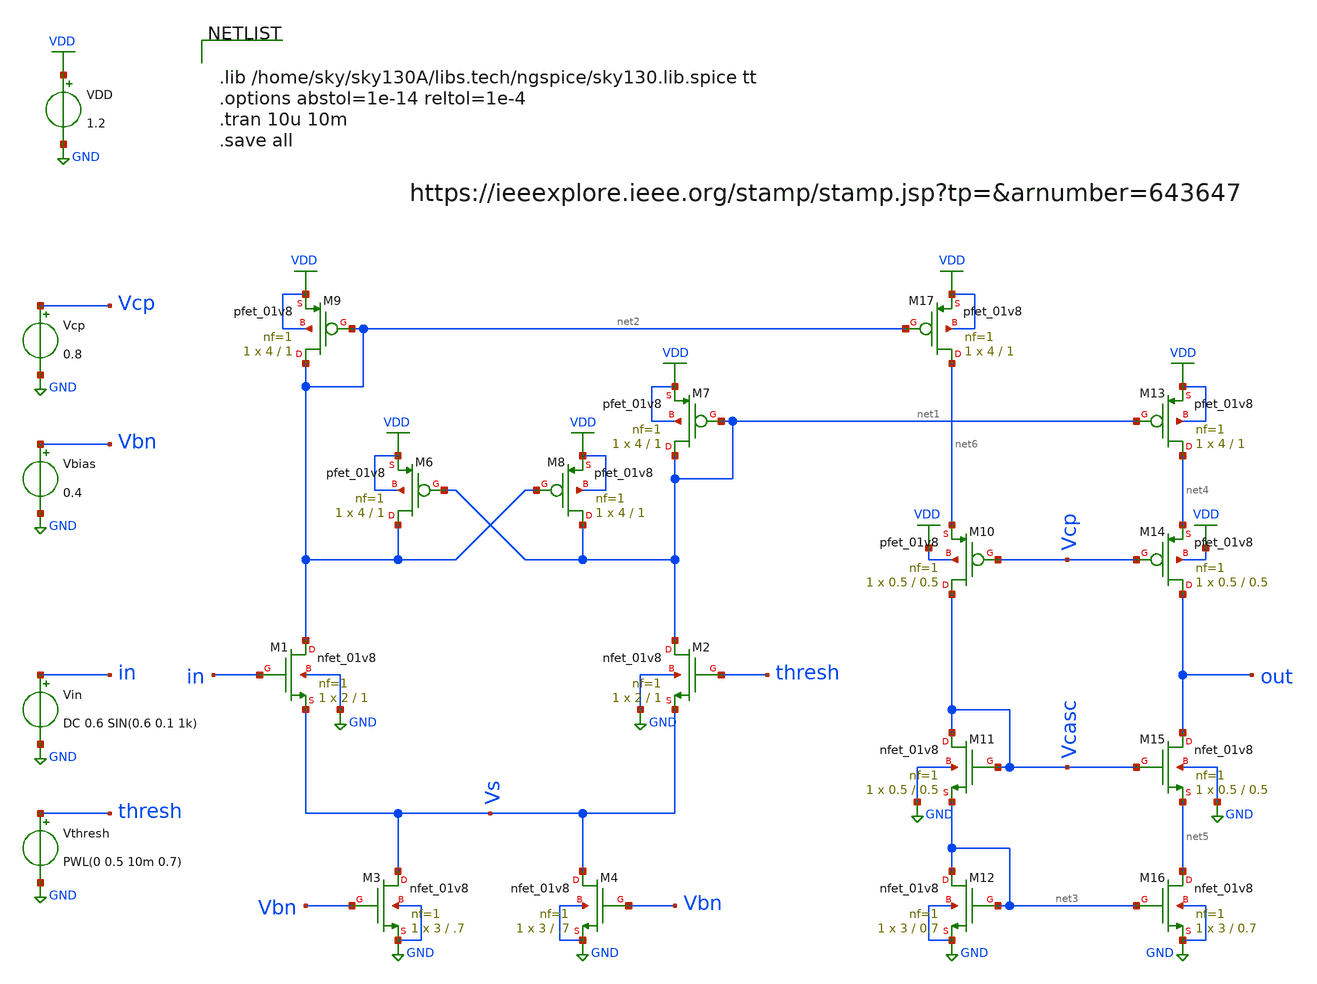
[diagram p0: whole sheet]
** sch_path: xschem/zcd/comparator_tb.sch
**.subckt comparator_tb
XM1 net2 in Vs GND sky130_fd_pr__nfet_01v8 L=1 W=2 nf=1 ad='int((nf+1)/2) * W/nf * 0.29' as='int((nf+2)/2) * W/nf * 0.29'
+ pd='2*int((nf+1)/2) * (W/nf + 0.29)' ps='2*int((nf+2)/2) * (W/nf + 0.29)' nrd='0.29 / W' nrs='0.29 / W'
+ sa=0 sb=0 sd=0 mult=1 m=1
VDD VDD GND 1.2
XM2 net1 thresh Vs GND sky130_fd_pr__nfet_01v8 L=1 W=2 nf=1 ad='int((nf+1)/2) * W/nf * 0.29' as='int((nf+2)/2) * W/nf * 0.29'
+ pd='2*int((nf+1)/2) * (W/nf + 0.29)' ps='2*int((nf+2)/2) * (W/nf + 0.29)' nrd='0.29 / W' nrs='0.29 / W'
+ sa=0 sb=0 sd=0 mult=1 m=1
XM3 Vs Vbn GND GND sky130_fd_pr__nfet_01v8 L=.7 W=3 nf=1 ad='int((nf+1)/2) * W/nf * 0.29' as='int((nf+2)/2) * W/nf * 0.29'
+ pd='2*int((nf+1)/2) * (W/nf + 0.29)' ps='2*int((nf+2)/2) * (W/nf + 0.29)' nrd='0.29 / W' nrs='0.29 / W'
+ sa=0 sb=0 sd=0 mult=1 m=1
XM4 Vs Vbn GND GND sky130_fd_pr__nfet_01v8 L=.7 W=3 nf=1 ad='int((nf+1)/2) * W/nf * 0.29' as='int((nf+2)/2) * W/nf * 0.29'
+ pd='2*int((nf+1)/2) * (W/nf + 0.29)' ps='2*int((nf+2)/2) * (W/nf + 0.29)' nrd='0.29 / W' nrs='0.29 / W'
+ sa=0 sb=0 sd=0 mult=1 m=1
XM6 net2 net1 VDD VDD sky130_fd_pr__pfet_01v8 L=1 W=4 nf=1 ad='int((nf+1)/2) * W/nf * 0.29' as='int((nf+2)/2) * W/nf * 0.29'
+ pd='2*int((nf+1)/2) * (W/nf + 0.29)' ps='2*int((nf+2)/2) * (W/nf + 0.29)' nrd='0.29 / W' nrs='0.29 / W'
+ sa=0 sb=0 sd=0 mult=1 m=1
XM7 net1 net1 VDD VDD sky130_fd_pr__pfet_01v8 L=1 W=4 nf=1 ad='int((nf+1)/2) * W/nf * 0.29' as='int((nf+2)/2) * W/nf * 0.29'
+ pd='2*int((nf+1)/2) * (W/nf + 0.29)' ps='2*int((nf+2)/2) * (W/nf + 0.29)' nrd='0.29 / W' nrs='0.29 / W'
+ sa=0 sb=0 sd=0 mult=1 m=1
XM8 net1 net2 VDD VDD sky130_fd_pr__pfet_01v8 L=1 W=4 nf=1 ad='int((nf+1)/2) * W/nf * 0.29' as='int((nf+2)/2) * W/nf * 0.29'
+ pd='2*int((nf+1)/2) * (W/nf + 0.29)' ps='2*int((nf+2)/2) * (W/nf + 0.29)' nrd='0.29 / W' nrs='0.29 / W'
+ sa=0 sb=0 sd=0 mult=1 m=1
XM9 net2 net2 VDD VDD sky130_fd_pr__pfet_01v8 L=1 W=4 nf=1 ad='int((nf+1)/2) * W/nf * 0.29' as='int((nf+2)/2) * W/nf * 0.29'
+ pd='2*int((nf+1)/2) * (W/nf + 0.29)' ps='2*int((nf+2)/2) * (W/nf + 0.29)' nrd='0.29 / W' nrs='0.29 / W'
+ sa=0 sb=0 sd=0 mult=1 m=1
XM10 Vcasc Vcp net6 VDD sky130_fd_pr__pfet_01v8 L=0.5 W=0.5 nf=1 ad='int((nf+1)/2) * W/nf * 0.29' as='int((nf+2)/2) * W/nf * 0.29'
+ pd='2*int((nf+1)/2) * (W/nf + 0.29)' ps='2*int((nf+2)/2) * (W/nf + 0.29)' nrd='0.29 / W' nrs='0.29 / W'
+ sa=0 sb=0 sd=0 mult=1 m=1
XM11 Vcasc Vcasc net3 GND sky130_fd_pr__nfet_01v8 L=0.5 W=0.5 nf=1 ad='int((nf+1)/2) * W/nf * 0.29' as='int((nf+2)/2) * W/nf * 0.29'
+ pd='2*int((nf+1)/2) * (W/nf + 0.29)' ps='2*int((nf+2)/2) * (W/nf + 0.29)' nrd='0.29 / W' nrs='0.29 / W'
+ sa=0 sb=0 sd=0 mult=1 m=1
XM12 net3 net3 GND GND sky130_fd_pr__nfet_01v8 L=0.7 W=3 nf=1 ad='int((nf+1)/2) * W/nf * 0.29' as='int((nf+2)/2) * W/nf * 0.29'
+ pd='2*int((nf+1)/2) * (W/nf + 0.29)' ps='2*int((nf+2)/2) * (W/nf + 0.29)' nrd='0.29 / W' nrs='0.29 / W'
+ sa=0 sb=0 sd=0 mult=1 m=1
XM13 net4 net1 VDD VDD sky130_fd_pr__pfet_01v8 L=1 W=4 nf=1 ad='int((nf+1)/2) * W/nf * 0.29' as='int((nf+2)/2) * W/nf * 0.29'
+ pd='2*int((nf+1)/2) * (W/nf + 0.29)' ps='2*int((nf+2)/2) * (W/nf + 0.29)' nrd='0.29 / W' nrs='0.29 / W'
+ sa=0 sb=0 sd=0 mult=1 m=1
XM14 out Vcp net4 VDD sky130_fd_pr__pfet_01v8 L=0.5 W=0.5 nf=1 ad='int((nf+1)/2) * W/nf * 0.29' as='int((nf+2)/2) * W/nf * 0.29'
+ pd='2*int((nf+1)/2) * (W/nf + 0.29)' ps='2*int((nf+2)/2) * (W/nf + 0.29)' nrd='0.29 / W' nrs='0.29 / W'
+ sa=0 sb=0 sd=0 mult=1 m=1
XM15 out Vcasc net5 GND sky130_fd_pr__nfet_01v8 L=0.5 W=0.5 nf=1 ad='int((nf+1)/2) * W/nf * 0.29' as='int((nf+2)/2) * W/nf * 0.29'
+ pd='2*int((nf+1)/2) * (W/nf + 0.29)' ps='2*int((nf+2)/2) * (W/nf + 0.29)' nrd='0.29 / W' nrs='0.29 / W'
+ sa=0 sb=0 sd=0 mult=1 m=1
XM16 net5 net3 GND GND sky130_fd_pr__nfet_01v8 L=0.7 W=3 nf=1 ad='int((nf+1)/2) * W/nf * 0.29' as='int((nf+2)/2) * W/nf * 0.29'
+ pd='2*int((nf+1)/2) * (W/nf + 0.29)' ps='2*int((nf+2)/2) * (W/nf + 0.29)' nrd='0.29 / W' nrs='0.29 / W'
+ sa=0 sb=0 sd=0 mult=1 m=1
XM17 net6 net2 VDD VDD sky130_fd_pr__pfet_01v8 L=1 W=4 nf=1 ad='int((nf+1)/2) * W/nf * 0.29' as='int((nf+2)/2) * W/nf * 0.29'
+ pd='2*int((nf+1)/2) * (W/nf + 0.29)' ps='2*int((nf+2)/2) * (W/nf + 0.29)' nrd='0.29 / W' nrs='0.29 / W'
+ sa=0 sb=0 sd=0 mult=1 m=1
Vbias Vbn GND 0.4
Vcp Vcp GND 0.8
Vthresh thresh GND PWL(0 0.5 10m 0.7)
Vin in GND DC 0.6 SIN(0.6 0.1 1k)
**** begin user architecture code


.lib /home/sky/sky130A/libs.tech/ngspice/sky130.lib.spice tt
.options abstol=1e-14 reltol=1e-4
.tran 10u 10m
.save all


**** end user architecture code
**.ends
.GLOBAL GND
.GLOBAL VDD
.end
